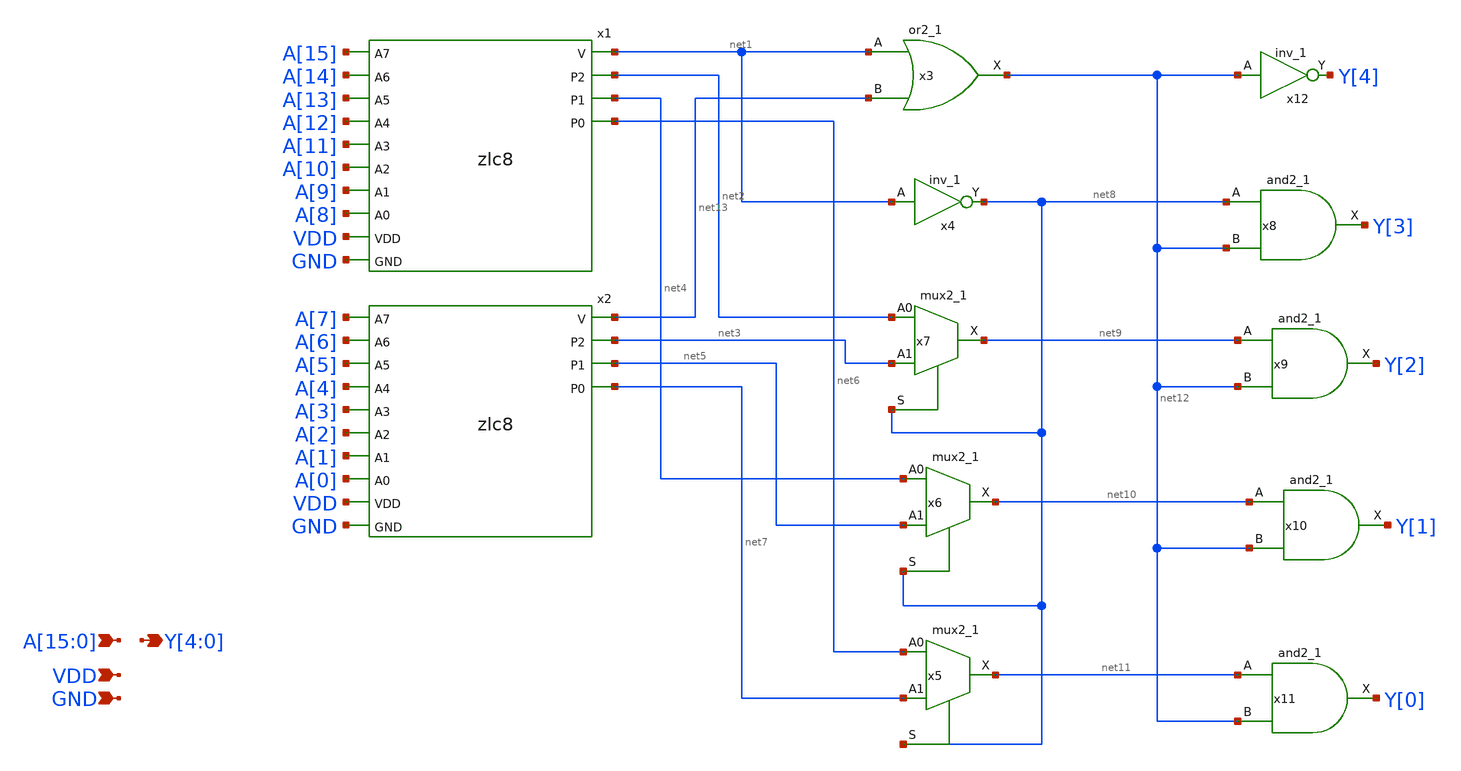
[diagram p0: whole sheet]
** sch_path: xschem/zlc16.sch
**.subckt zlc16 VDD GND
*+ A[15],A[14],A[13],A[12],A[11],A[10],A[9],A[8],A[7],A[6],A[5],A[4],A[3],A[2],A[1],A[0] Y[4],Y[3],Y[2],Y[1],Y[0]
*.ipin VDD
*.ipin GND
*.ipin A[15],A[14],A[13],A[12],A[11],A[10],A[9],A[8],A[7],A[6],A[5],A[4],A[3],A[2],A[1],A[0]
*.opin Y[4],Y[3],Y[2],Y[1],Y[0]
x3 net1 net13 GND GND VDD VDD net12 sky130_fd_sc_hd__or2_1
x4 net1 GND GND VDD VDD net8 sky130_fd_sc_hd__inv_1
x5 net6 net7 net8 GND GND VDD VDD net11 sky130_fd_sc_hd__mux2_1
x6 net4 net5 net8 GND GND VDD VDD net10 sky130_fd_sc_hd__mux2_1
x7 net2 net3 net8 GND GND VDD VDD net9 sky130_fd_sc_hd__mux2_1
x8 net8 net12 GND GND VDD VDD Y[3] sky130_fd_sc_hd__and2_1
x9 net9 net12 GND GND VDD VDD Y[2] sky130_fd_sc_hd__and2_1
x10 net10 net12 GND GND VDD VDD Y[1] sky130_fd_sc_hd__and2_1
x11 net11 net12 GND GND VDD VDD Y[0] sky130_fd_sc_hd__and2_1
x12 net12 GND GND VDD VDD Y[4] sky130_fd_sc_hd__inv_1
x1 A[15] A[14] net1 A[13] A[12] net2 A[11] A[10] net4 A[9] A[8] net6 VDD GND zlc8
x2 A[7] A[6] net13 A[5] A[4] net3 A[3] A[2] net5 A[1] A[0] net7 VDD GND zlc8
**.ends

* expanding   symbol:  zlc8.sym # of pins=14
** sym_path: xschem/zlc8.sym
** sch_path: xschem/zlc8.sch
.subckt zlc8 A7 A6 V A5 A4 P2 A3 A2 P1 A1 A0 P0 VDD GND
*.ipin A7
*.ipin A6
*.ipin A5
*.ipin A4
*.ipin A3
*.ipin A2
*.ipin A1
*.ipin A0
*.opin V
*.opin P2
*.opin P1
*.opin P0
*.ipin VDD
*.ipin GND
x3 net1 net3 GND GND VDD VDD V sky130_fd_sc_hd__or2_1
x4 net1 GND GND VDD VDD P2 sky130_fd_sc_hd__inv_1
x5 net2 net4 P2 GND GND VDD VDD P1 sky130_fd_sc_hd__mux2_1
x6 net5 net6 P2 GND GND VDD VDD P0 sky130_fd_sc_hd__mux2_1
x1 A7 net1 A6 net2 A5 A4 net5 VDD GND zlc4
x2 A3 net3 A2 net4 A1 A0 net6 VDD GND zlc4
.ends


* expanding   symbol:  zlc4.sym # of pins=9
** sym_path: xschem/zlc4.sym
** sch_path: xschem/zlc4.sch
.subckt zlc4 A3 V A2 P1 A1 A0 P0 VDD GND
*.ipin A3
*.ipin A2
*.ipin A1
*.ipin A0
*.opin V
*.opin P1
*.opin P0
*.ipin VDD
*.ipin GND
x3 net1 net2 GND GND VDD VDD V sky130_fd_sc_hd__or2_1
x4 net1 GND GND VDD VDD P1 sky130_fd_sc_hd__inv_1
x5 net3 net4 P1 GND GND VDD VDD P0 sky130_fd_sc_hd__mux2_1
x1 A3 net1 A2 net3 VDD GND zlc2
x2 A1 net2 A0 net4 VDD GND zlc2
.ends


* expanding   symbol:  zlc2.sym # of pins=6
** sym_path: xschem/zlc2.sym
** sch_path: xschem/zlc2.sch
.subckt zlc2 HI V LO P VDD GND
*.ipin HI
*.ipin LO
*.opin V
*.opin P
*.ipin VDD
*.ipin GND
x1 HI LO GND GND VDD VDD V sky130_fd_sc_hd__or2_1
x2 HI GND GND VDD VDD P sky130_fd_sc_hd__inv_1
.ends

.end
